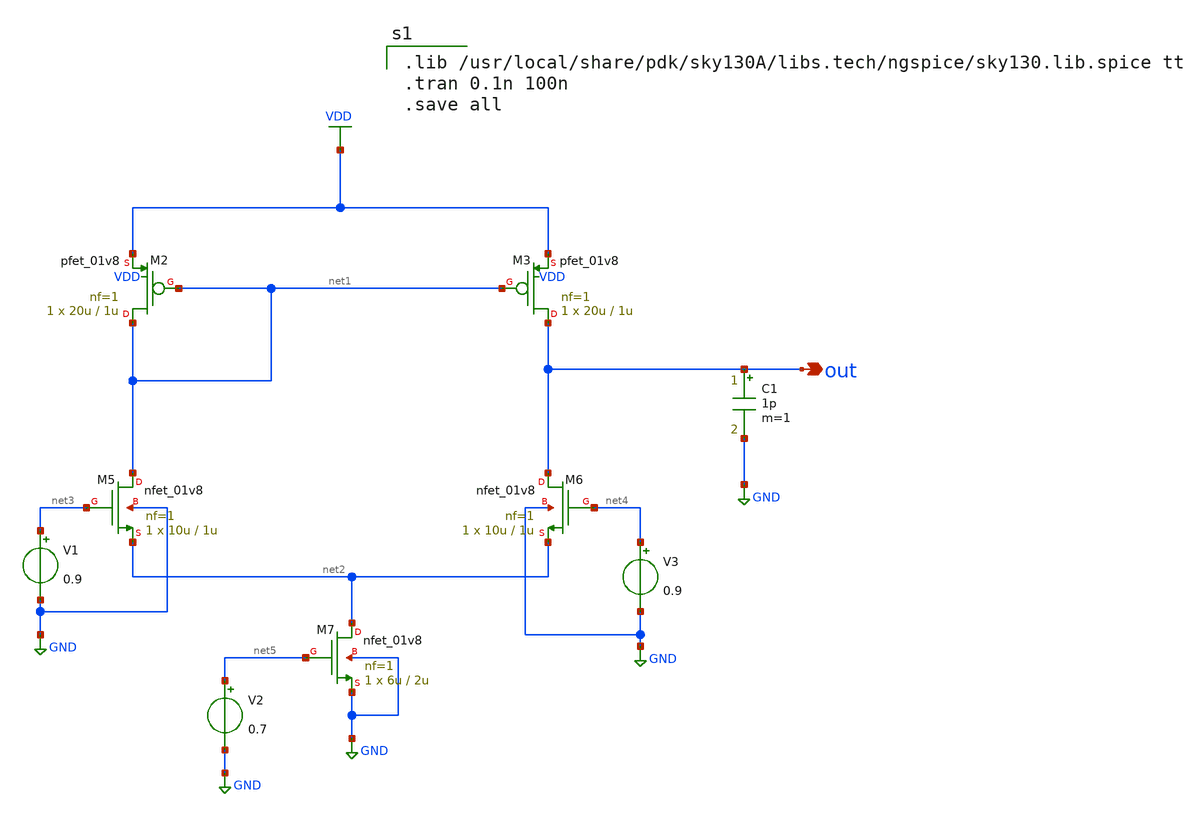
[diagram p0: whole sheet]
** sch_path: 5t_opamp/5t_opamp.sch
**.subckt 5t_opamp out
*.opin out
XM3 out net1 VDD VDD sky130_fd_pr__pfet_01v8 L=1u W=20u nf=1 ad='int((1 + 1)/2) * 20u / 1 * 0.29' as='int((1 + 2)/2) * 20u / 1 * 0.29'
+ pd='2*int((1 + 1)/2) * (20u / 1 + 0.29)' ps='2*int((1 + 2)/2) * (20u / 1 + 0.29)' nrd='0.29 / 20u ' nrs='0.29 / 20u '
+ sa=0 sb=0 sd=0 mult=1 m=1
XM5 net1 net3 net2 GND sky130_fd_pr__nfet_01v8 L=1u W=10u nf=1 ad='int((1 + 1)/2) * 10u / 1 * 0.29' as='int((1 + 2)/2) * 10u / 1 * 0.29'
+ pd='2*int((1 + 1)/2) * (10u / 1 + 0.29)' ps='2*int((1 + 2)/2) * (10u / 1 + 0.29)' nrd='0.29 / 10u ' nrs='0.29 / 10u '
+ sa=0 sb=0 sd=0 mult=1 m=1
XM6 out net4 net2 GND sky130_fd_pr__nfet_01v8 L=1u W=10u nf=1 ad='int((1 + 1)/2) * 10u / 1 * 0.29' as='int((1 + 2)/2) * 10u / 1 * 0.29'
+ pd='2*int((1 + 1)/2) * (10u / 1 + 0.29)' ps='2*int((1 + 2)/2) * (10u / 1 + 0.29)' nrd='0.29 / 10u ' nrs='0.29 / 10u '
+ sa=0 sb=0 sd=0 mult=1 m=1
XM7 net2 net5 GND GND sky130_fd_pr__nfet_01v8 L=2u W=6u nf=1 ad='int((1 + 1)/2) * 6u / 1 * 0.29' as='int((1 + 2)/2) * 6u / 1 * 0.29'
+ pd='2*int((1 + 1)/2) * (6u / 1 + 0.29)' ps='2*int((1 + 2)/2) * (6u / 1 + 0.29)' nrd='0.29 / 6u ' nrs='0.29 / 6u '
+ sa=0 sb=0 sd=0 mult=1 m=1
MM2 net1 net1 VDD VDD sky130_fd_pr__pfet_01v8 L=1u W=20u nf=1 ad='int((1 + 1)/2) * 20u / 1 * 0.29' as='int((1 + 2)/2) * 20u / 1 * 0.29'
+ pd='2*int((1 + 1)/2) * (20u / 1 + 0.29)' ps='2*int((1 + 2)/2) * (20u / 1 + 0.29)' nrd='0.29 / 20u ' nrs='0.29 / 20u '
+ sa=0 sb=0 sd=0 mult=1 m=1
C1 out GND 1p m=1
V1 net3 GND 0.9
V2 net5 GND 0.7
V3 net4 GND 0.9
**** begin user architecture code

.lib /usr/local/share/pdk/sky130A/libs.tech/ngspice/sky130.lib.spice tt
.tran 0.1n 100n
.save all

**** end user architecture code
**.ends
.GLOBAL GND
.GLOBAL VDD
.end
